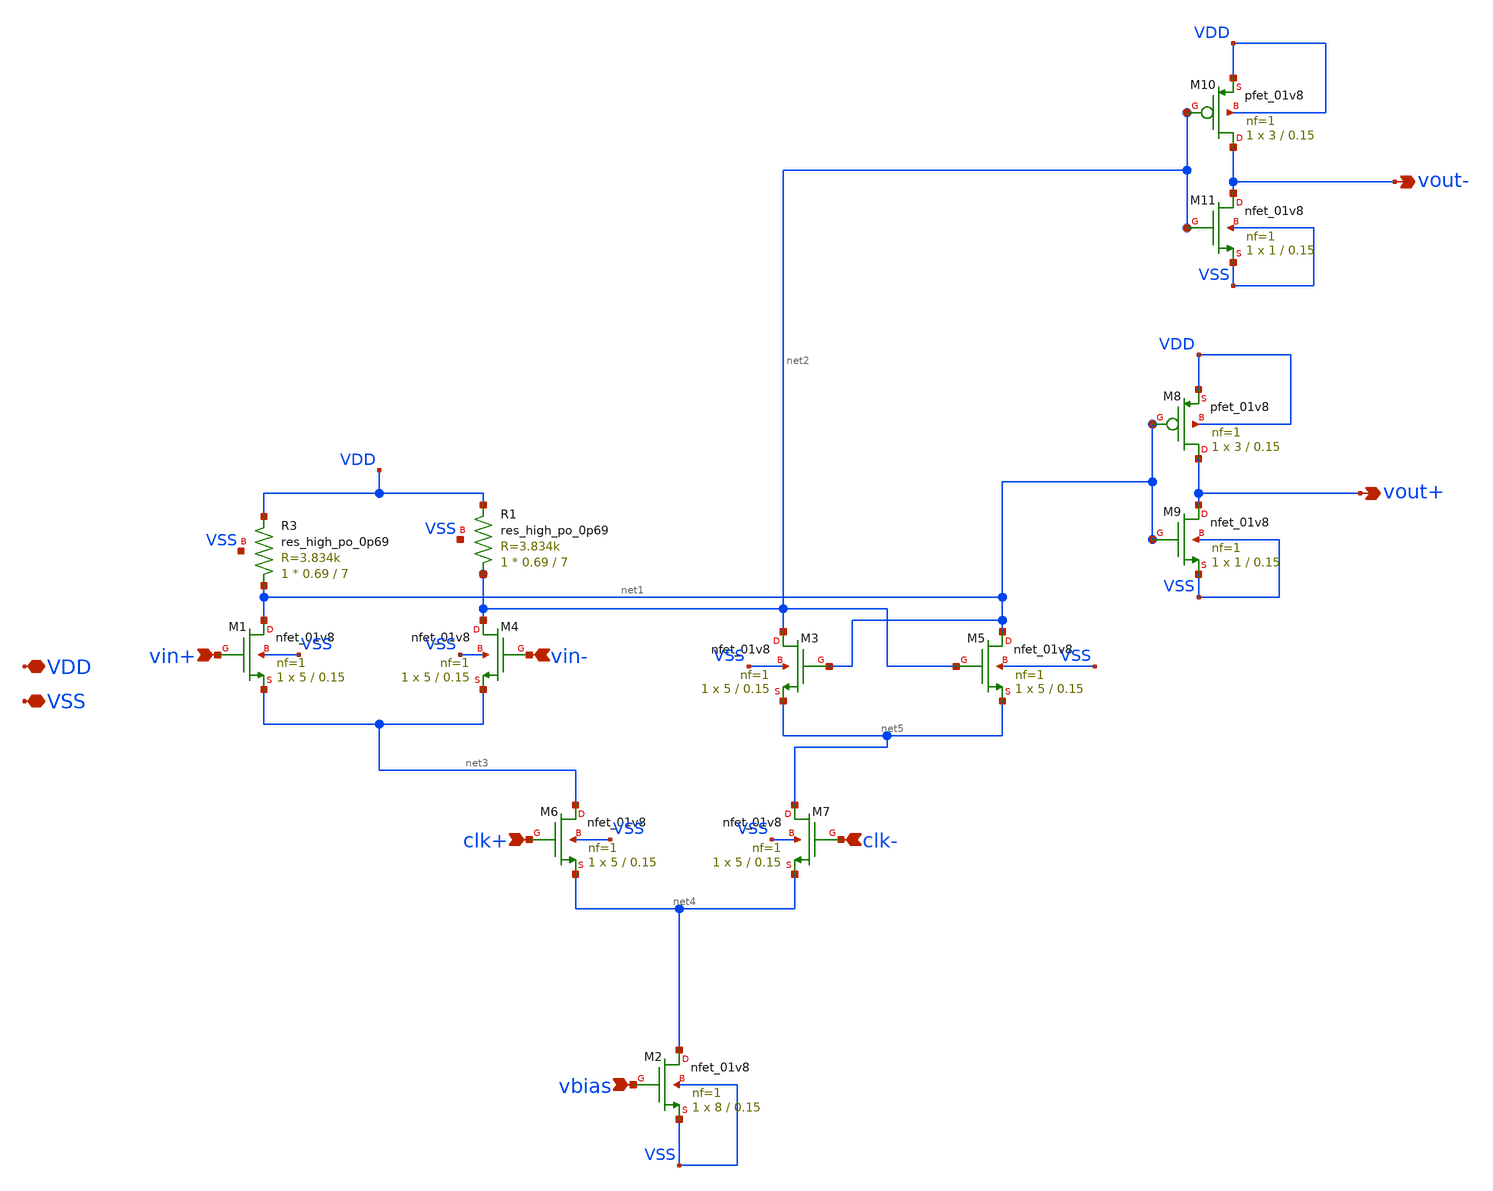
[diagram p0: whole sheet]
** sch_path: xschem/tuning/d_latch_tune.sch
**.subckt d_latch_tune VDD VSS vin+ clk- vbias vout+ clk+ vout- vin-
*.iopin VDD
*.iopin VSS
*.ipin vin+
*.ipin clk-
*.ipin vbias
*.opin vout+
*.ipin clk+
*.opin vout-
*.ipin vin-
XM1 net1 vin+ net3 VSS sky130_fd_pr__nfet_01v8 L=0.15 W=5 nf=1 ad='int((nf+1)/2) * W/nf * 0.29' as='int((nf+2)/2) * W/nf * 0.29'
+ pd='2*int((nf+1)/2) * (W/nf + 0.29)' ps='2*int((nf+2)/2) * (W/nf + 0.29)' nrd='0.29 / W' nrs='0.29 / W'
+ sa=0 sb=0 sd=0 mult=1 m=1
XM2 net4 vbias VSS VSS sky130_fd_pr__nfet_01v8 L=0.15 W=8 nf=1 ad='int((nf+1)/2) * W/nf * 0.29' as='int((nf+2)/2) * W/nf * 0.29'
+ pd='2*int((nf+1)/2) * (W/nf + 0.29)' ps='2*int((nf+2)/2) * (W/nf + 0.29)' nrd='0.29 / W' nrs='0.29 / W'
+ sa=0 sb=0 sd=0 mult=1 m=1
XM4 net2 vin- net3 VSS sky130_fd_pr__nfet_01v8 L=0.15 W=5 nf=1 ad='int((nf+1)/2) * W/nf * 0.29' as='int((nf+2)/2) * W/nf * 0.29'
+ pd='2*int((nf+1)/2) * (W/nf + 0.29)' ps='2*int((nf+2)/2) * (W/nf + 0.29)' nrd='0.29 / W' nrs='0.29 / W'
+ sa=0 sb=0 sd=0 mult=1 m=1
XM3 net2 net1 net5 VSS sky130_fd_pr__nfet_01v8 L=0.15 W=5 nf=1 ad='int((nf+1)/2) * W/nf * 0.29' as='int((nf+2)/2) * W/nf * 0.29'
+ pd='2*int((nf+1)/2) * (W/nf + 0.29)' ps='2*int((nf+2)/2) * (W/nf + 0.29)' nrd='0.29 / W' nrs='0.29 / W'
+ sa=0 sb=0 sd=0 mult=1 m=1
XM5 net1 net2 net5 VSS sky130_fd_pr__nfet_01v8 L=0.15 W=5 nf=1 ad='int((nf+1)/2) * W/nf * 0.29' as='int((nf+2)/2) * W/nf * 0.29'
+ pd='2*int((nf+1)/2) * (W/nf + 0.29)' ps='2*int((nf+2)/2) * (W/nf + 0.29)' nrd='0.29 / W' nrs='0.29 / W'
+ sa=0 sb=0 sd=0 mult=1 m=1
XM6 net3 clk+ net4 VSS sky130_fd_pr__nfet_01v8 L=0.15 W=5 nf=1 ad='int((nf+1)/2) * W/nf * 0.29' as='int((nf+2)/2) * W/nf * 0.29'
+ pd='2*int((nf+1)/2) * (W/nf + 0.29)' ps='2*int((nf+2)/2) * (W/nf + 0.29)' nrd='0.29 / W' nrs='0.29 / W'
+ sa=0 sb=0 sd=0 mult=1 m=1
XM7 net5 clk- net4 VSS sky130_fd_pr__nfet_01v8 L=0.15 W=5 nf=1 ad='int((nf+1)/2) * W/nf * 0.29' as='int((nf+2)/2) * W/nf * 0.29'
+ pd='2*int((nf+1)/2) * (W/nf + 0.29)' ps='2*int((nf+2)/2) * (W/nf + 0.29)' nrd='0.29 / W' nrs='0.29 / W'
+ sa=0 sb=0 sd=0 mult=1 m=1
XM8 vout+ net1 VDD VDD sky130_fd_pr__pfet_01v8 L=0.15 W=3 nf=1 ad='int((nf+1)/2) * W/nf * 0.29' as='int((nf+2)/2) * W/nf * 0.29'
+ pd='2*int((nf+1)/2) * (W/nf + 0.29)' ps='2*int((nf+2)/2) * (W/nf + 0.29)' nrd='0.29 / W' nrs='0.29 / W'
+ sa=0 sb=0 sd=0 mult=1 m=1
XM9 vout+ net1 VSS VSS sky130_fd_pr__nfet_01v8 L=0.15 W=1 nf=1 ad='int((nf+1)/2) * W/nf * 0.29' as='int((nf+2)/2) * W/nf * 0.29'
+ pd='2*int((nf+1)/2) * (W/nf + 0.29)' ps='2*int((nf+2)/2) * (W/nf + 0.29)' nrd='0.29 / W' nrs='0.29 / W'
+ sa=0 sb=0 sd=0 mult=1 m=1
XM10 vout- net2 VDD VDD sky130_fd_pr__pfet_01v8 L=0.15 W=3 nf=1 ad='int((nf+1)/2) * W/nf * 0.29' as='int((nf+2)/2) * W/nf * 0.29'
+ pd='2*int((nf+1)/2) * (W/nf + 0.29)' ps='2*int((nf+2)/2) * (W/nf + 0.29)' nrd='0.29 / W' nrs='0.29 / W'
+ sa=0 sb=0 sd=0 mult=1 m=1
XM11 vout- net2 VSS VSS sky130_fd_pr__nfet_01v8 L=0.15 W=1 nf=1 ad='int((nf+1)/2) * W/nf * 0.29' as='int((nf+2)/2) * W/nf * 0.29'
+ pd='2*int((nf+1)/2) * (W/nf + 0.29)' ps='2*int((nf+2)/2) * (W/nf + 0.29)' nrd='0.29 / W' nrs='0.29 / W'
+ sa=0 sb=0 sd=0 mult=1 m=1
XR3 net1 VDD VSS sky130_fd_pr__res_high_po_0p69 L=7 mult=1 m=1
XR1 net2 VDD VSS sky130_fd_pr__res_high_po_0p69 L=7 mult=1 m=1
**.ends
.end
